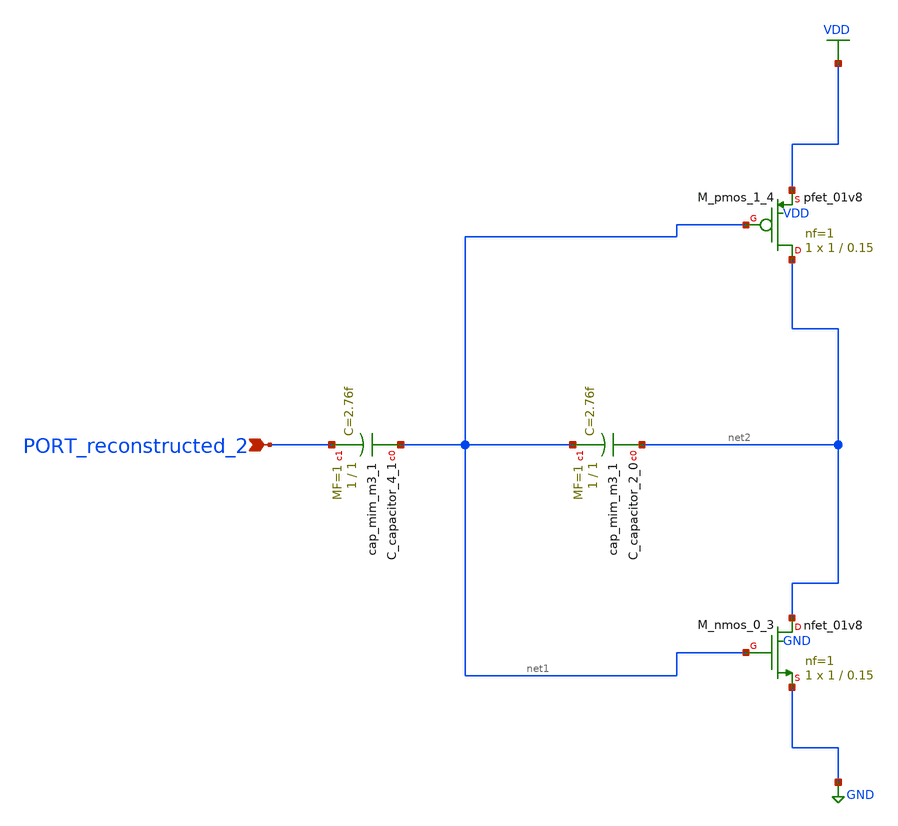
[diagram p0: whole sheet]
** sch_path: schematics/AMSNet/407.sch
**.subckt 407 PORT_reconstructed_2
*.ipin PORT_reconstructed_2
XC_capacitor_2_0 net2 net1 sky130_fd_pr__cap_mim_m3_1 W=1 L=1 MF=1 m=1
XC_capacitor_4_1 net1 PORT_reconstructed_2 sky130_fd_pr__cap_mim_m3_1 W=1 L=1 MF=1 m=1
XM_nmos_0_3 net2 net1 GND GND sky130_fd_pr__nfet_01v8 L=0.15 W=1 nf=1 ad='int((1 + 1)/2) * 1 / 1 * 0.29'
+ as='int((1 + 2)/2) * 1 / 1 * 0.29' pd='2*int((1 + 1)/2) * (1 / 1 + 0.29)' ps='2*int((1 + 2)/2) * (1 / 1 + 0.29)'
+ nrd='0.29 / 1 ' nrs='0.29 / 1 ' sa=0 sb=0 sd=0 mult=1 m=1
XM_pmos_1_4 net2 net1 VDD VDD sky130_fd_pr__pfet_01v8 L=0.15 W=1 nf=1 ad='int((1 + 1)/2) * 1 / 1 * 0.29'
+ as='int((1 + 2)/2) * 1 / 1 * 0.29' pd='2*int((1 + 1)/2) * (1 / 1 + 0.29)' ps='2*int((1 + 2)/2) * (1 / 1 + 0.29)'
+ nrd='0.29 / 1 ' nrs='0.29 / 1 ' sa=0 sb=0 sd=0 mult=1 m=1
**.ends
.GLOBAL GND
.GLOBAL VDD
.end
